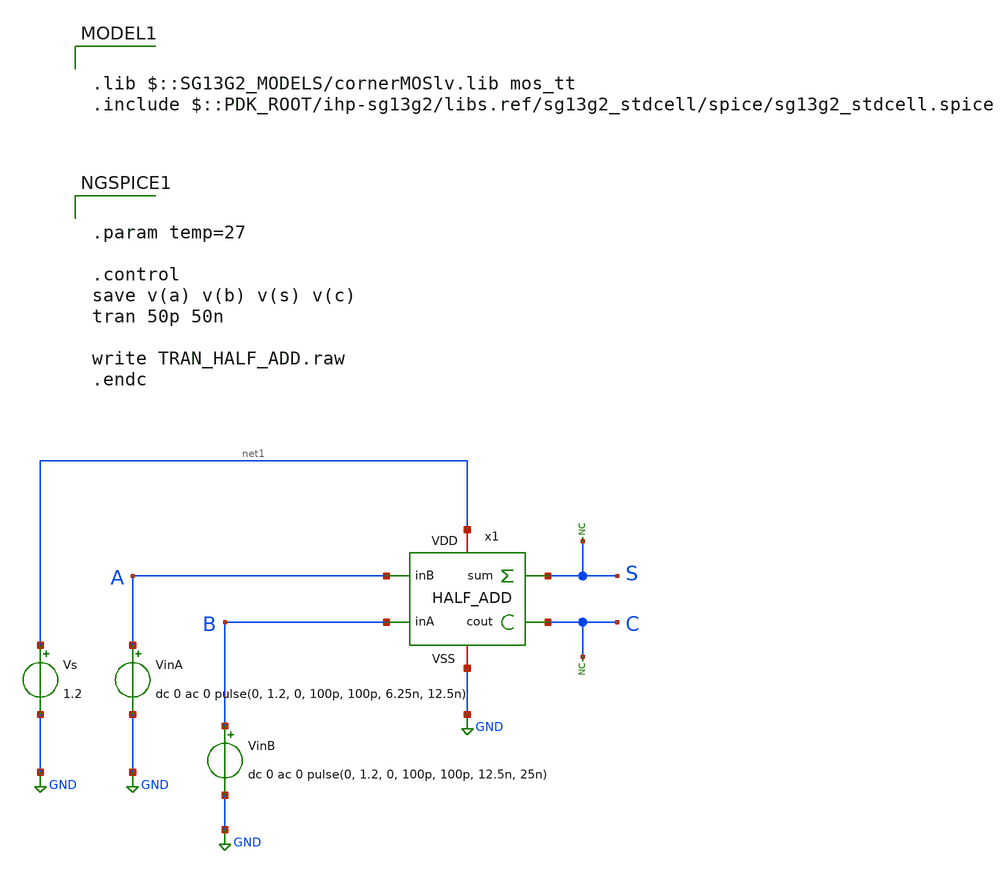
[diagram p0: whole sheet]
** sch_path: 30_MHz_Fractional_N_PLL/design_data/xschem/HALF_ADD_TB.sch

.lib $::SG13G2_MODELS/cornerMOSlv.lib mos_tt
.include $::PDK_ROOT/ihp-sg13g2/libs.ref/sg13g2_stdcell/spice/sg13g2_stdcell.spice

**.subckt HALF_ADD_TB
VinA A GND dc 0 ac 0 pulse(0, 1.2, 0, 100p, 100p, 6.25n, 12.5n)
VinB B GND dc 0 ac 0 pulse(0, 1.2, 0, 100p, 100p, 12.5n, 25n)
Vs net1 GND 1.2
* noconn S
* noconn C
x1 A S B net1 GND C HALF_ADD
**** begin user architecture code


.param temp=27

.control
save v(a) v(b) v(s) v(c)
tran 50p 50n

write TRAN_HALF_ADD.raw
.endc


**** end user architecture code
**.ends

* expanding   symbol:  HALF_ADD.sym # of pins=6
** sym_path: 30_MHz_Fractional_N_PLL/design_data/xschem/HALF_ADD.sym
** sch_path: 30_MHz_Fractional_N_PLL/design_data/xschem/HALF_ADD.sch
.subckt HALF_ADD inB sum inA VDD VSS cout
*.ipin inA
*.ipin inB
*.opin sum
*.opin cout
*.iopin VSS
*.iopin VDD
x1 sum inA inB VDD VSS sg13g2_xor2_1
x2 cout inA inB VDD VSS sg13g2_and2_1
.ends


* expanding   symbol:  sg13g2_stdcells/sg13g2_xor2_1.sym # of pins=3
** sym_path: sg13g2_stdcells/sg13g2_xor2_1.sym
** sch_path: sg13g2_stdcells/sg13g2_xor2_1.sch
.subckt sg13g2_xor2_1 X A B VDD VSS
*.opin X
*.ipin B
*.ipin A
*.iopin VDD
*.iopin VSS
XM1 net1 A VSS VSS sg13_lv_nmos w=550.00n l=130.00n ng=1 m=1 mm_ok=1
XM2 net1 B VSS VSS sg13_lv_nmos w=550.00n l=130.00n ng=1 m=1 mm_ok=1
XM3 X net1 VSS VSS sg13_lv_nmos w=740.00n l=130.00n ng=1 m=1 mm_ok=1
XM4 X B net3 VSS sg13_lv_nmos w=740.00n l=130.00n ng=1 m=1 mm_ok=1
XM5 net3 A VSS VSS sg13_lv_nmos w=740.00n l=130.00n ng=1 m=1 mm_ok=1
XM6 net4 A VDD VDD sg13_lv_pmos w=1.000u l=130.00n ng=1 m=1 mm_ok=1
XM7 net1 B net4 VDD sg13_lv_pmos w=1.000u l=130.00n ng=1 m=1 mm_ok=1
XM8 net2 A VDD VDD sg13_lv_pmos w=1.12u l=130.00n ng=1 m=1 mm_ok=1
XM9 X net1 net2 VDD sg13_lv_pmos w=1.12u l=130.00n ng=1 m=1 mm_ok=1
XM10 net2 B VDD VDD sg13_lv_pmos w=1.12u l=130.00n ng=1 m=1 mm_ok=1
.ends


* expanding   symbol:  sg13g2_stdcells/sg13g2_and2_1.sym # of pins=3
** sym_path: sg13g2_stdcells/sg13g2_and2_1.sym
** sch_path: sg13g2_stdcells/sg13g2_and2_1.sch
.subckt sg13g2_and2_1 X A B VDD VSS
*.ipin A
*.ipin B
*.opin X
*.iopin VDD
*.iopin VSS
XM1 net1 A net2 VSS sg13_lv_nmos w=640.00n l=130.00n ng=1 m=1 mm_ok=1
XM2 net2 B VSS VSS sg13_lv_nmos w=640.00n l=130.00n ng=1 m=1 mm_ok=1
XM3 X net1 VSS VSS sg13_lv_nmos w=740.00n l=130.00n ng=1 m=1 mm_ok=1
XM4 net1 B VDD VDD sg13_lv_pmos w=840.00n l=130.00n ng=1 m=1 mm_ok=1
XM5 net1 A VDD VDD sg13_lv_pmos w=840.00n l=130.00n ng=1 m=1 mm_ok=1
XM6 X net1 VDD VDD sg13_lv_pmos w=1.12u l=130.00n ng=1 m=1 mm_ok=1
.ends

.GLOBAL GND
.end
